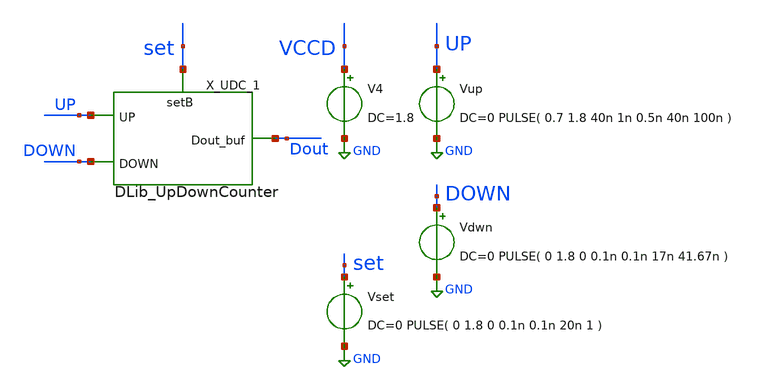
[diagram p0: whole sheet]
** sch_path: xschem/tb/UpDonwCounter_tb.sch
**.subckt UpDonwCounter_tb
X_UDC_1 UP DOWN set GND GND VCCD VCCD Dout DLib_UpDownCounter
Vup UP GND DC=0 PULSE( 0.7 1.8 40n 1n 0.5n 40n 100n )
Vdwn DOWN GND DC=0 PULSE( 0 1.8 0 0.1n 0.1n 17n 41.67n )
Vset set GND DC=0 PULSE( 0 1.8 0 0.1n 0.1n 20n 1 )
V4 VCCD GND DC=1.8
**** begin user architecture code


** Library on VNU server
.lib /home/dkits/efabless/mpw-5/pdks/sky130A/libs.tech/ngspice/sky130.lib.spice tt
.inc /home/dkits/efabless/mpw-5/pdks/sky130A/libs.ref/sky130_fd_sc_hd/spice/sky130_fd_sc_hd.spice
** Library on Home PC
*.lib /home/dkit/efabless/pdks/sky130A/libs.tech/ngspice/sky130.lib.spice tt
*.inc /home/dkit/efabless/pdks/sky130A/libs.ref/sky130_fd_sc_hd/spice/sky130_fd_sc_hd.spice



.param mc_mm_switch=0
.control
   TRAN 0.1n 10u
   plot set/2+3 UP/2+2 Down/2+1 Dout/2+0.05
.endc


**** end user architecture code
**.ends
.GLOBAL GND
.end
